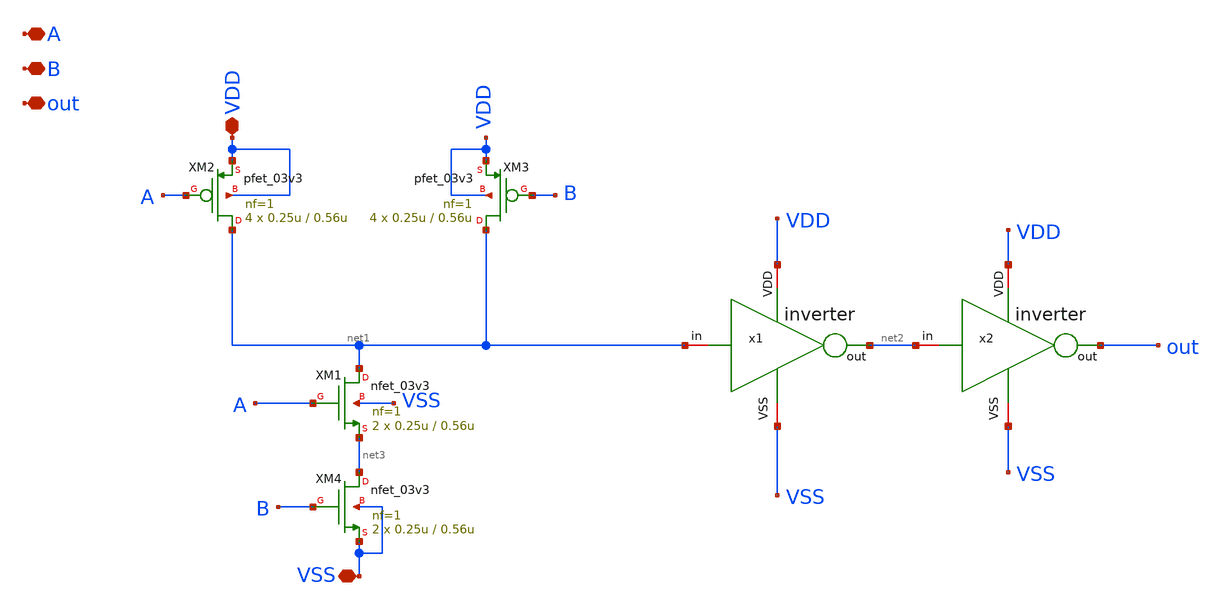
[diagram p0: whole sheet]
** sch_path: designs/sar_adc/digital/nand_edge/xschem/NAND.sch
**.subckt NAND VDD A B out VSS
*.iopin VDD
*.iopin A
*.iopin B
*.iopin out
*.iopin VSS
XM2 net1 A VDD VDD pfet_03v3 L=0.56u W=0.25u nf=1 ad='int((nf+1)/2) * W/nf * 0.18u' as='int((nf+2)/2) * W/nf * 0.18u'
+ pd='2*int((nf+1)/2) * (W/nf + 0.18u)' ps='2*int((nf+2)/2) * (W/nf + 0.18u)' nrd='0.18u / W' nrs='0.18u / W'
+ sa=0 sb=0 sd=0 m=4
XM1 net1 A net3 VSS nfet_03v3 L=0.56u W=0.25u nf=1 ad='int((nf+1)/2) * W/nf * 0.18u' as='int((nf+2)/2) * W/nf * 0.18u'
+ pd='2*int((nf+1)/2) * (W/nf + 0.18u)' ps='2*int((nf+2)/2) * (W/nf + 0.18u)' nrd='0.18u / W' nrs='0.18u / W'
+ sa=0 sb=0 sd=0 m=2
XM3 net1 B VDD VDD pfet_03v3 L=0.56u W=0.25u nf=1 ad='int((nf+1)/2) * W/nf * 0.18u' as='int((nf+2)/2) * W/nf * 0.18u'
+ pd='2*int((nf+1)/2) * (W/nf + 0.18u)' ps='2*int((nf+2)/2) * (W/nf + 0.18u)' nrd='0.18u / W' nrs='0.18u / W'
+ sa=0 sb=0 sd=0 m=4
XM4 net3 B VSS VSS nfet_03v3 L=0.56u W=0.25u nf=1 ad='int((nf+1)/2) * W/nf * 0.18u' as='int((nf+2)/2) * W/nf * 0.18u'
+ pd='2*int((nf+1)/2) * (W/nf + 0.18u)' ps='2*int((nf+2)/2) * (W/nf + 0.18u)' nrd='0.18u / W' nrs='0.18u / W'
+ sa=0 sb=0 sd=0 m=2
x1 VDD net1 net2 VSS inverter
x2 VDD net2 out VSS inverter
**.ends

* expanding   symbol:  sar_adc/digital/buffer_inv_x1/xschem/inverter.sym # of pins=6
** sym_path: designs/sar_adc/digital/buffer_inv_x1/xschem/inverter.sym
** sch_path: designs/sar_adc/digital/buffer_inv_x1/xschem/inverter.sch
.subckt inverter VDD in out VSS
*.opin out
*.iopin in
*.iopin VDD
*.iopin VSS
XM1 out in VSS VSS nfet_03v3 L=0.56u W=0.25u nf=1 ad='int((nf+1)/2) * W/nf * 0.18u' as='int((nf+2)/2) * W/nf * 0.18u'
+ pd='2*int((nf+1)/2) * (W/nf + 0.18u)' ps='2*int((nf+2)/2) * (W/nf + 0.18u)' nrd='0.18u / W' nrs='0.18u / W'
+ sa=0 sb=0 sd=0 m=2
XM2 out in VDD VDD pfet_03v3 L=0.56u W=0.25u nf=1 ad='int((nf+1)/2) * W/nf * 0.18u' as='int((nf+2)/2) * W/nf * 0.18u'
+ pd='2*int((nf+1)/2) * (W/nf + 0.18u)' ps='2*int((nf+2)/2) * (W/nf + 0.18u)' nrd='0.18u / W' nrs='0.18u / W'
+ sa=0 sb=0 sd=0 m=4
.ends

.end
